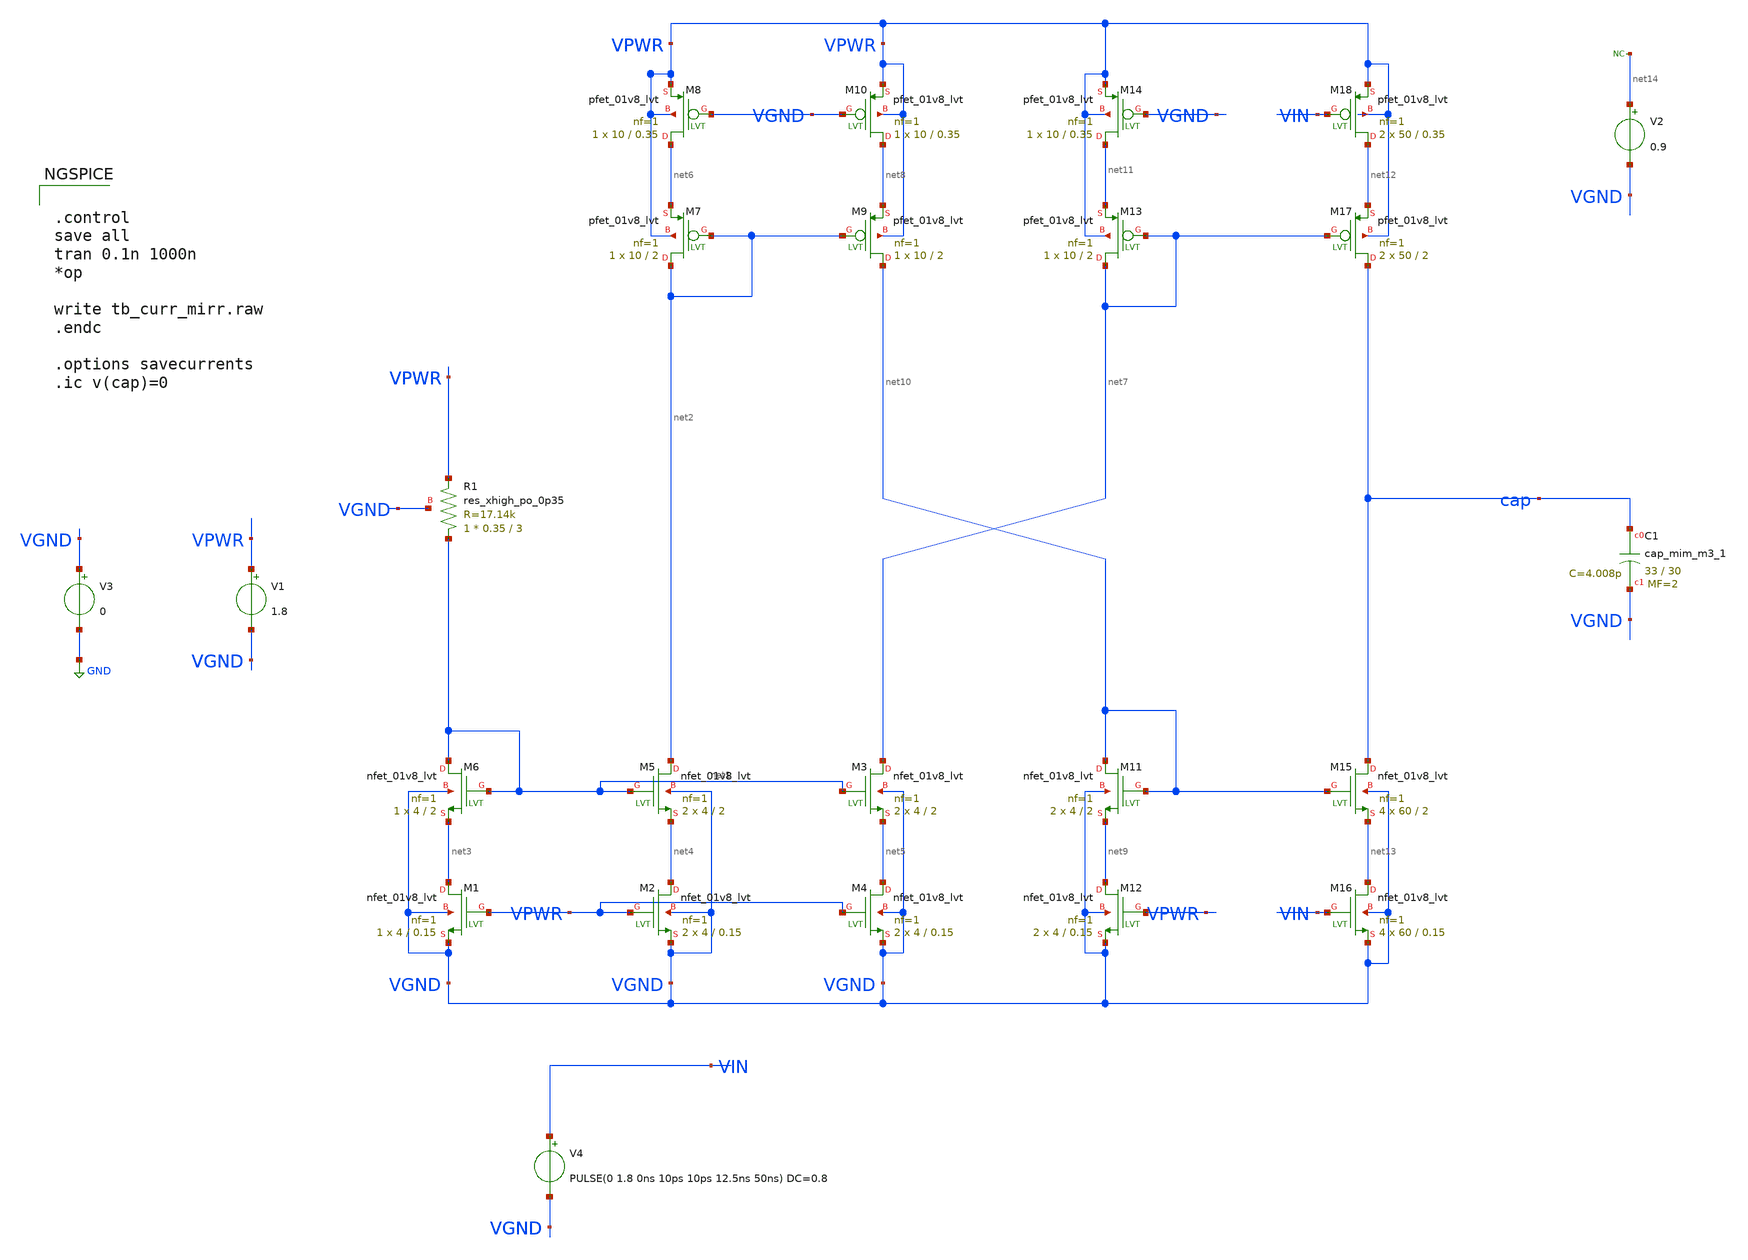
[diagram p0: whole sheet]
** sch_path: design/tb_curr_mirr_large.sch
**.subckt tb_curr_mirr_large
V1 VPWR VGND 1.8
V3 VGND GND 0
XM5 net2 net1 net4 VGND sky130_fd_pr__nfet_01v8_lvt L=2 W=4 nf=1 ad='int((nf+1)/2) * W/nf * 0.29' as='int((nf+2)/2) * W/nf * 0.29'
+ pd='2*int((nf+1)/2) * (W/nf + 0.29)' ps='2*int((nf+2)/2) * (W/nf + 0.29)' nrd='0.29 / W' nrs='0.29 / W'
+ sa=0 sb=0 sd=0 mult=2 m=2
XM6 net1 net1 net3 VGND sky130_fd_pr__nfet_01v8_lvt L=2 W=4 nf=1 ad='int((nf+1)/2) * W/nf * 0.29' as='int((nf+2)/2) * W/nf * 0.29'
+ pd='2*int((nf+1)/2) * (W/nf + 0.29)' ps='2*int((nf+2)/2) * (W/nf + 0.29)' nrd='0.29 / W' nrs='0.29 / W'
+ sa=0 sb=0 sd=0 mult=1 m=1
XR1 net1 VPWR VGND sky130_fd_pr__res_xhigh_po_0p35 L=3 mult=1 m=1
XM1 net3 VPWR VGND VGND sky130_fd_pr__nfet_01v8_lvt L=0.15 W=4 nf=1 ad='int((nf+1)/2) * W/nf * 0.29'
+ as='int((nf+2)/2) * W/nf * 0.29' pd='2*int((nf+1)/2) * (W/nf + 0.29)' ps='2*int((nf+2)/2) * (W/nf + 0.29)'
+ nrd='0.29 / W' nrs='0.29 / W' sa=0 sb=0 sd=0 mult=1 m=1
XM2 net4 VPWR VGND VGND sky130_fd_pr__nfet_01v8_lvt L=0.15 W=4 nf=1 ad='int((nf+1)/2) * W/nf * 0.29'
+ as='int((nf+2)/2) * W/nf * 0.29' pd='2*int((nf+1)/2) * (W/nf + 0.29)' ps='2*int((nf+2)/2) * (W/nf + 0.29)'
+ nrd='0.29 / W' nrs='0.29 / W' sa=0 sb=0 sd=0 mult=2 m=2
XM3 net7 net1 net5 VGND sky130_fd_pr__nfet_01v8_lvt L=2 W=4 nf=1 ad='int((nf+1)/2) * W/nf * 0.29' as='int((nf+2)/2) * W/nf * 0.29'
+ pd='2*int((nf+1)/2) * (W/nf + 0.29)' ps='2*int((nf+2)/2) * (W/nf + 0.29)' nrd='0.29 / W' nrs='0.29 / W'
+ sa=0 sb=0 sd=0 mult=2 m=2
XM4 net5 VPWR VGND VGND sky130_fd_pr__nfet_01v8_lvt L=0.15 W=4 nf=1 ad='int((nf+1)/2) * W/nf * 0.29'
+ as='int((nf+2)/2) * W/nf * 0.29' pd='2*int((nf+1)/2) * (W/nf + 0.29)' ps='2*int((nf+2)/2) * (W/nf + 0.29)'
+ nrd='0.29 / W' nrs='0.29 / W' sa=0 sb=0 sd=0 mult=2 m=2
XM7 net2 net2 net6 VPWR sky130_fd_pr__pfet_01v8_lvt L=2 W=10 nf=1 ad='int((nf+1)/2) * W/nf * 0.29' as='int((nf+2)/2) * W/nf * 0.29'
+ pd='2*int((nf+1)/2) * (W/nf + 0.29)' ps='2*int((nf+2)/2) * (W/nf + 0.29)' nrd='0.29 / W' nrs='0.29 / W'
+ sa=0 sb=0 sd=0 mult=1 m=1
XM8 net6 VGND VPWR VPWR sky130_fd_pr__pfet_01v8_lvt L=0.35 W=10 nf=1 ad='int((nf+1)/2) * W/nf * 0.29'
+ as='int((nf+2)/2) * W/nf * 0.29' pd='2*int((nf+1)/2) * (W/nf + 0.29)' ps='2*int((nf+2)/2) * (W/nf + 0.29)'
+ nrd='0.29 / W' nrs='0.29 / W' sa=0 sb=0 sd=0 mult=1 m=1
XM9 net10 net2 net8 VPWR sky130_fd_pr__pfet_01v8_lvt L=2 W=10 nf=1 ad='int((nf+1)/2) * W/nf * 0.29' as='int((nf+2)/2) * W/nf * 0.29'
+ pd='2*int((nf+1)/2) * (W/nf + 0.29)' ps='2*int((nf+2)/2) * (W/nf + 0.29)' nrd='0.29 / W' nrs='0.29 / W'
+ sa=0 sb=0 sd=0 mult=1 m=1
XM10 net8 VGND VPWR VPWR sky130_fd_pr__pfet_01v8_lvt L=0.35 W=10 nf=1 ad='int((nf+1)/2) * W/nf * 0.29'
+ as='int((nf+2)/2) * W/nf * 0.29' pd='2*int((nf+1)/2) * (W/nf + 0.29)' ps='2*int((nf+2)/2) * (W/nf + 0.29)'
+ nrd='0.29 / W' nrs='0.29 / W' sa=0 sb=0 sd=0 mult=1 m=1
XM11 net10 net10 net9 VGND sky130_fd_pr__nfet_01v8_lvt L=2 W=4 nf=1 ad='int((nf+1)/2) * W/nf * 0.29'
+ as='int((nf+2)/2) * W/nf * 0.29' pd='2*int((nf+1)/2) * (W/nf + 0.29)' ps='2*int((nf+2)/2) * (W/nf + 0.29)'
+ nrd='0.29 / W' nrs='0.29 / W' sa=0 sb=0 sd=0 mult=2 m=2
XM12 net9 VPWR VGND VGND sky130_fd_pr__nfet_01v8_lvt L=0.15 W=4 nf=1 ad='int((nf+1)/2) * W/nf * 0.29'
+ as='int((nf+2)/2) * W/nf * 0.29' pd='2*int((nf+1)/2) * (W/nf + 0.29)' ps='2*int((nf+2)/2) * (W/nf + 0.29)'
+ nrd='0.29 / W' nrs='0.29 / W' sa=0 sb=0 sd=0 mult=2 m=2
XM13 net7 net7 net11 VPWR sky130_fd_pr__pfet_01v8_lvt L=2 W=10 nf=1 ad='int((nf+1)/2) * W/nf * 0.29'
+ as='int((nf+2)/2) * W/nf * 0.29' pd='2*int((nf+1)/2) * (W/nf + 0.29)' ps='2*int((nf+2)/2) * (W/nf + 0.29)'
+ nrd='0.29 / W' nrs='0.29 / W' sa=0 sb=0 sd=0 mult=1 m=1
XM14 net11 VGND VPWR VPWR sky130_fd_pr__pfet_01v8_lvt L=0.35 W=10 nf=1 ad='int((nf+1)/2) * W/nf * 0.29'
+ as='int((nf+2)/2) * W/nf * 0.29' pd='2*int((nf+1)/2) * (W/nf + 0.29)' ps='2*int((nf+2)/2) * (W/nf + 0.29)'
+ nrd='0.29 / W' nrs='0.29 / W' sa=0 sb=0 sd=0 mult=1 m=1
XM15 cap net10 net13 VGND sky130_fd_pr__nfet_01v8_lvt L=2 W=60 nf=1 ad='int((nf+1)/2) * W/nf * 0.29'
+ as='int((nf+2)/2) * W/nf * 0.29' pd='2*int((nf+1)/2) * (W/nf + 0.29)' ps='2*int((nf+2)/2) * (W/nf + 0.29)'
+ nrd='0.29 / W' nrs='0.29 / W' sa=0 sb=0 sd=0 mult=4 m=4
XM17 cap net7 net12 VPWR sky130_fd_pr__pfet_01v8_lvt L=2 W=50 nf=1 ad='int((nf+1)/2) * W/nf * 0.29' as='int((nf+2)/2) * W/nf * 0.29'
+ pd='2*int((nf+1)/2) * (W/nf + 0.29)' ps='2*int((nf+2)/2) * (W/nf + 0.29)' nrd='0.29 / W' nrs='0.29 / W'
+ sa=0 sb=0 sd=0 mult=2 m=2
XM18 net12 VIN VPWR VPWR sky130_fd_pr__pfet_01v8_lvt L=0.35 W=50 nf=1 ad='int((nf+1)/2) * W/nf * 0.29'
+ as='int((nf+2)/2) * W/nf * 0.29' pd='2*int((nf+1)/2) * (W/nf + 0.29)' ps='2*int((nf+2)/2) * (W/nf + 0.29)'
+ nrd='0.29 / W' nrs='0.29 / W' sa=0 sb=0 sd=0 mult=2 m=2
V2 net14 VGND 0.9
V4 VIN VGND PULSE(0 1.8 0ns 10ps 10ps 12.5ns 50ns) DC=0.8
XM16 net13 VIN VGND VGND sky130_fd_pr__nfet_01v8_lvt L=0.15 W=60 nf=1 ad='int((nf+1)/2) * W/nf * 0.29'
+ as='int((nf+2)/2) * W/nf * 0.29' pd='2*int((nf+1)/2) * (W/nf + 0.29)' ps='2*int((nf+2)/2) * (W/nf + 0.29)'
+ nrd='0.29 / W' nrs='0.29 / W' sa=0 sb=0 sd=0 mult=4 m=4
XC1 cap VGND sky130_fd_pr__cap_mim_m3_1 W=33 L=30 MF=2 m=2
* noconn #net14
**** begin user architecture code

** opencircuitdesign pdks install
.lib $::SKYWATER_MODELS/sky130.lib.spice tt
.include $::SKYWATER_STDCELLS/sky130_fd_sc_hd.spice




.control
save all
tran 0.1n 1000n
*op

write tb_curr_mirr.raw
.endc

.options savecurrents
.ic v(cap)=0


**** end user architecture code
**.ends
.GLOBAL GND
.end
